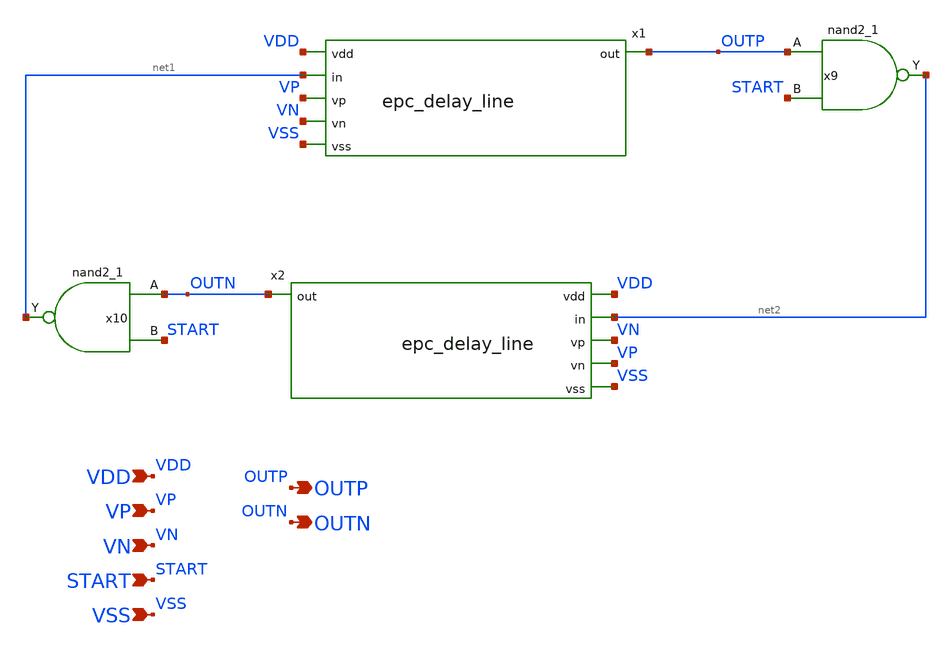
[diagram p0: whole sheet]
** sch_path: xschem/epc.sch
**.subckt epc VDD VP VN VSS OUTP START OUTN
*.ipin VDD
*.ipin VP
*.ipin VN
*.ipin VSS
*.opin OUTP
*.ipin START
*.opin OUTN
x9 OUTP START VSS VSS VDD VDD net2 sky130_fd_sc_hd__nand2_1
x10 OUTN START VSS VSS VDD VDD net1 sky130_fd_sc_hd__nand2_1
x1 VDD net1 VP VN VSS OUTP epc_delay_line
x2 VDD net2 VN VP VSS OUTN epc_delay_line
**.ends

* expanding   symbol:  epc_delay_line.sym # of pins=6
** sym_path: epc_delay_line.sym
** sch_path: epc_delay_line.sch
.subckt epc_delay_line vdd in vp vn vss out
*.ipin vdd
*.ipin in
*.ipin vp
*.ipin vn
*.ipin vss
*.opin out
x1 vdd in net1 vp vss epc_delay
x2 vdd net1 net3 vn vss epc_delay
x3 vdd net3 net2 vp vss epc_delay
x4 vdd net2 net7 vn vss epc_delay
x5 vdd net7 net4 vp vss epc_delay
x6 vdd net4 net6 vn vss epc_delay
x7 vdd net6 net5 vp vss epc_delay
x8 vdd net5 out vn vss epc_delay
.ends


* expanding   symbol:  epc_delay.sym # of pins=5
** sym_path: epc_delay.sym
** sch_path: epc_delay.sch
.subckt epc_delay VDD IN OUT VIN VSS
*.ipin VDD
*.ipin VIN
*.ipin IN
*.ipin VSS
*.opin OUT
.param W_N=0.5 L_N=0.5 W_P=1.0 L_P=0.5
XM1 net2 VIN VDD VDD sky130_fd_pr__pfet_01v8_lvt L=L_P W=W_P nf=1 ad='int((nf+1)/2) * W/nf * 0.29' as='int((nf+2)/2) * W/nf * 0.29'
+ pd='2*int((nf+1)/2) * (W/nf + 0.29)' ps='2*int((nf+2)/2) * (W/nf + 0.29)' nrd='0.29 / W' nrs='0.29 / W'
+ sa=0 sb=0 sd=0 mult=1 m=1
XM2 OUT IN net2 VDD sky130_fd_pr__pfet_01v8_lvt L=L_P W=W_P nf=1 ad='int((nf+1)/2) * W/nf * 0.29' as='int((nf+2)/2) * W/nf * 0.29'
+ pd='2*int((nf+1)/2) * (W/nf + 0.29)' ps='2*int((nf+2)/2) * (W/nf + 0.29)' nrd='0.29 / W' nrs='0.29 / W'
+ sa=0 sb=0 sd=0 mult=1 m=1
XM3 OUT IN net1 VSS sky130_fd_pr__nfet_01v8_lvt L=L_N W=W_N nf=1 ad='int((nf+1)/2) * W/nf * 0.29' as='int((nf+2)/2) * W/nf * 0.29'
+ pd='2*int((nf+1)/2) * (W/nf + 0.29)' ps='2*int((nf+2)/2) * (W/nf + 0.29)' nrd='0.29 / W' nrs='0.29 / W'
+ sa=0 sb=0 sd=0 mult=1 m=1
XM4 net1 VIN VSS VSS sky130_fd_pr__nfet_01v8_lvt L=L_N W=W_N nf=1 ad='int((nf+1)/2) * W/nf * 0.29' as='int((nf+2)/2) * W/nf * 0.29'
+ pd='2*int((nf+1)/2) * (W/nf + 0.29)' ps='2*int((nf+2)/2) * (W/nf + 0.29)' nrd='0.29 / W' nrs='0.29 / W'
+ sa=0 sb=0 sd=0 mult=1 m=1
.ends

.end
